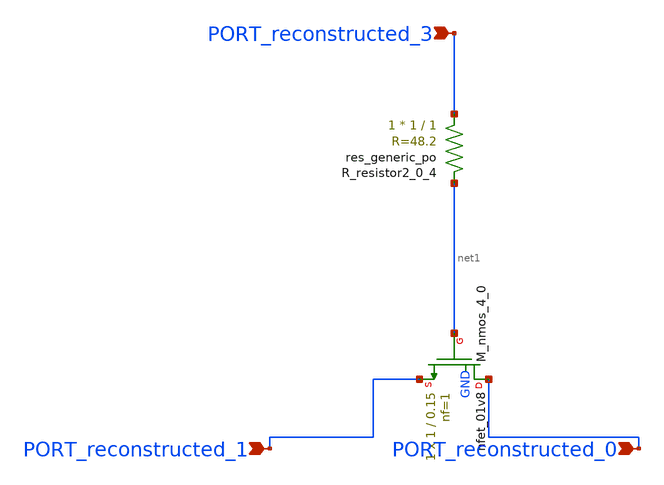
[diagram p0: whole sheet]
** sch_path: schematics/AMSNet/19.sch
**.subckt 19 PORT_reconstructed_1 PORT_reconstructed_3 PORT_reconstructed_0
*.ipin PORT_reconstructed_1
*.ipin PORT_reconstructed_3
*.ipin PORT_reconstructed_0
XM_nmos_4_0 PORT_reconstructed_0 net1 PORT_reconstructed_1 GND sky130_fd_pr__nfet_01v8 L=0.15 W=1 nf=1
+ ad='int((1 + 1)/2) * 1 / 1 * 0.29' as='int((1 + 2)/2) * 1 / 1 * 0.29' pd='2*int((1 + 1)/2) * (1 / 1 + 0.29)'
+ ps='2*int((1 + 2)/2) * (1 / 1 + 0.29)' nrd='0.29 / 1 ' nrs='0.29 / 1 ' sa=0 sb=0 sd=0 mult=1 m=1
XR_resistor2_0_4 PORT_reconstructed_3 net1 sky130_fd_pr__res_generic_po W=1 L=1 m=1
**.ends
.end
